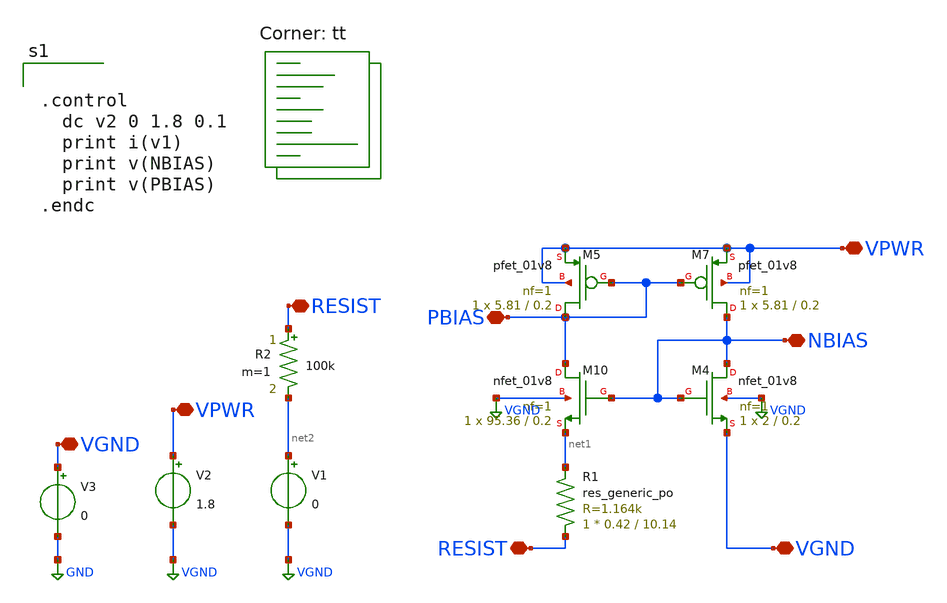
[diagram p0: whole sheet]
** sch_path: project2/sky130_hilas_Bootstrap01.sch
**.subckt sky130_hilas_Bootstrap01 VPWR NBIAS PBIAS VGND RESIST RESIST VPWR VGND
*.iopin VPWR
*.iopin NBIAS
*.iopin PBIAS
*.iopin VGND
*.iopin RESIST
*.iopin RESIST
*.iopin VPWR
*.iopin VGND
XM4 NBIAS NBIAS VGND VGND sky130_fd_pr__nfet_01v8 L=0.2 W=2 nf=1 ad='int((nf+1)/2) * W/nf * 0.29' as='int((nf+2)/2) * W/nf * 0.29'
+ pd='2*int((nf+1)/2) * (W/nf + 0.29)' ps='2*int((nf+2)/2) * (W/nf + 0.29)' nrd='0.29 / W' nrs='0.29 / W'
+ sa=0 sb=0 sd=0 mult=1 m=1
XM7 NBIAS PBIAS VPWR VPWR sky130_fd_pr__pfet_01v8 L=0.2 W=5.81 nf=1 ad='int((nf+1)/2) * W/nf * 0.29'
+ as='int((nf+2)/2) * W/nf * 0.29' pd='2*int((nf+1)/2) * (W/nf + 0.29)' ps='2*int((nf+2)/2) * (W/nf + 0.29)'
+ nrd='0.29 / W' nrs='0.29 / W' sa=0 sb=0 sd=0 mult=1 m=1
XM10 PBIAS NBIAS net1 VGND sky130_fd_pr__nfet_01v8 L=0.2 W=95.36 nf=1 ad='int((nf+1)/2) * W/nf * 0.29'
+ as='int((nf+2)/2) * W/nf * 0.29' pd='2*int((nf+1)/2) * (W/nf + 0.29)' ps='2*int((nf+2)/2) * (W/nf + 0.29)'
+ nrd='0.29 / W' nrs='0.29 / W' sa=0 sb=0 sd=0 mult=1 m=1
XM5 PBIAS PBIAS VPWR VPWR sky130_fd_pr__pfet_01v8 L=0.2 W=5.81 nf=1 ad='int((nf+1)/2) * W/nf * 0.29'
+ as='int((nf+2)/2) * W/nf * 0.29' pd='2*int((nf+1)/2) * (W/nf + 0.29)' ps='2*int((nf+2)/2) * (W/nf + 0.29)'
+ nrd='0.29 / W' nrs='0.29 / W' sa=0 sb=0 sd=0 mult=1 m=1
XR1 RESIST net1 sky130_fd_pr__res_generic_po W=0.42 L=10.14 m=1
V1 net2 VGND 0
V2 VPWR VGND 1.8
V3 VGND GND 0
R2 RESIST net2 100k m=1
**** begin user architecture code


.control
  dc v2 0 1.8 0.1
  print i(v1)
  print v(NBIAS)
  print v(PBIAS)
.endc


.lib $::SKYWATER_MODELS/sky130.lib.spice tt
**** end user architecture code
**.ends
.GLOBAL VGND
.GLOBAL GND
.end
